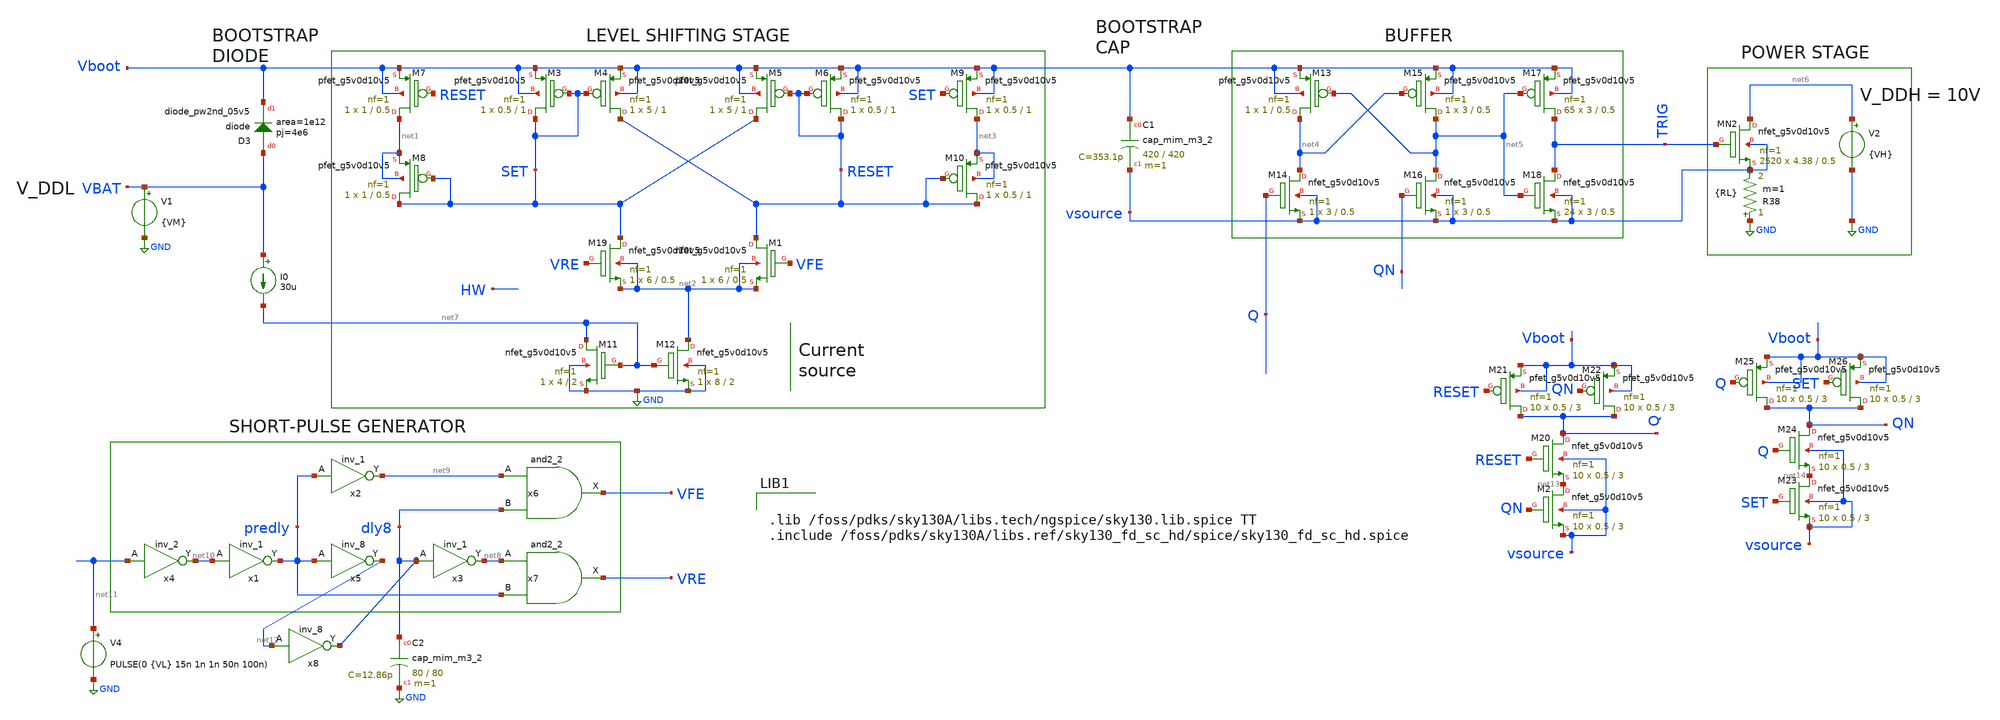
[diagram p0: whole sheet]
** sch_path: LS_boot_20230921/sch/LS_boot_latest_jm.sch
**.subckt LS_boot_latest_jm
XM7 net1 RESET Vboot Vboot sky130_fd_pr__pfet_g5v0d10v5 L=0.5 W=1 nf=1 ad='int((nf+1)/2) * W/nf * 0.29'
+ as='int((nf+2)/2) * W/nf * 0.29' pd='2*int((nf+1)/2) * (W/nf + 0.29)' ps='2*int((nf+2)/2) * (W/nf + 0.29)'
+ nrd='0.29 / W' nrs='0.29 / W' sa=0 sb=0 sd=0 mult=1 m=1
XM8 SET SET net1 net1 sky130_fd_pr__pfet_g5v0d10v5 L=0.5 W=1 nf=1 ad='int((nf+1)/2) * W/nf * 0.29' as='int((nf+2)/2) * W/nf * 0.29'
+ pd='2*int((nf+1)/2) * (W/nf + 0.29)' ps='2*int((nf+2)/2) * (W/nf + 0.29)' nrd='0.29 / W' nrs='0.29 / W'
+ sa=0 sb=0 sd=0 mult=1 m=1
XM4 RESET SET Vboot Vboot sky130_fd_pr__pfet_g5v0d10v5 L=1 W=5 nf=1 ad='int((nf+1)/2) * W/nf * 0.29'
+ as='int((nf+2)/2) * W/nf * 0.29' pd='2*int((nf+1)/2) * (W/nf + 0.29)' ps='2*int((nf+2)/2) * (W/nf + 0.29)'
+ nrd='0.29 / W' nrs='0.29 / W' sa=0 sb=0 sd=0 mult=1 m=1
XM3 SET SET Vboot Vboot sky130_fd_pr__pfet_g5v0d10v5 L=1 W=0.5 nf=1 ad='int((nf+1)/2) * W/nf * 0.29'
+ as='int((nf+2)/2) * W/nf * 0.29' pd='2*int((nf+1)/2) * (W/nf + 0.29)' ps='2*int((nf+2)/2) * (W/nf + 0.29)'
+ nrd='0.29 / W' nrs='0.29 / W' sa=0 sb=0 sd=0 mult=1 m=1
XM9 net3 SET Vboot Vboot sky130_fd_pr__pfet_g5v0d10v5 L=1 W=0.5 nf=1 ad='int((nf+1)/2) * W/nf * 0.29'
+ as='int((nf+2)/2) * W/nf * 0.29' pd='2*int((nf+1)/2) * (W/nf + 0.29)' ps='2*int((nf+2)/2) * (W/nf + 0.29)'
+ nrd='0.29 / W' nrs='0.29 / W' sa=0 sb=0 sd=0 mult=1 m=1
XM10 RESET RESET net3 net3 sky130_fd_pr__pfet_g5v0d10v5 L=1 W=0.5 nf=1 ad='int((nf+1)/2) * W/nf * 0.29'
+ as='int((nf+2)/2) * W/nf * 0.29' pd='2*int((nf+1)/2) * (W/nf + 0.29)' ps='2*int((nf+2)/2) * (W/nf + 0.29)'
+ nrd='0.29 / W' nrs='0.29 / W' sa=0 sb=0 sd=0 mult=1 m=1
XM5 SET RESET Vboot Vboot sky130_fd_pr__pfet_g5v0d10v5 L=1 W=5 nf=1 ad='int((nf+1)/2) * W/nf * 0.29'
+ as='int((nf+2)/2) * W/nf * 0.29' pd='2*int((nf+1)/2) * (W/nf + 0.29)' ps='2*int((nf+2)/2) * (W/nf + 0.29)'
+ nrd='0.29 / W' nrs='0.29 / W' sa=0 sb=0 sd=0 mult=1 m=1
XM6 RESET RESET Vboot Vboot sky130_fd_pr__pfet_g5v0d10v5 L=1 W=0.5 nf=1 ad='int((nf+1)/2) * W/nf * 0.29'
+ as='int((nf+2)/2) * W/nf * 0.29' pd='2*int((nf+1)/2) * (W/nf + 0.29)' ps='2*int((nf+2)/2) * (W/nf + 0.29)'
+ nrd='0.29 / W' nrs='0.29 / W' sa=0 sb=0 sd=0 mult=1 m=1
XD3 VBAT Vboot sky130_fd_pr__diode_pw2nd_05v5 area=1e12 pj=4e6
I0 VBAT net7 30u
x1 net10 VGND VNB VPB VPWR predly sky130_fd_sc_hd__inv_1
x2 predly VGND VNB VPB VPWR net9 sky130_fd_sc_hd__inv_1
x3 dly8 VGND VNB VPB VPWR net8 sky130_fd_sc_hd__inv_1
x4 net11 VGND VNB VPB VPWR net10 sky130_fd_sc_hd__inv_2
x5 predly VGND VNB VPB VPWR net12 sky130_fd_sc_hd__inv_8
x6 net9 dly8 VGND VNB VPB VPWR VFE sky130_fd_sc_hd__and2_2
x7 net8 predly VGND VNB VPB VPWR VRE sky130_fd_sc_hd__and2_2
XC1 Vboot vsource sky130_fd_pr__cap_mim_m3_2 W=420 L=420 MF=1 m=1
XM15 net5 net4 Vboot Vboot sky130_fd_pr__pfet_g5v0d10v5 L=0.5 W=3 nf=1 ad='int((nf+1)/2) * W/nf * 0.29'
+ as='int((nf+2)/2) * W/nf * 0.29' pd='2*int((nf+1)/2) * (W/nf + 0.29)' ps='2*int((nf+2)/2) * (W/nf + 0.29)'
+ nrd='0.29 / W' nrs='0.29 / W' sa=0 sb=0 sd=0 mult=1 m=1
XM13 net4 net5 Vboot Vboot sky130_fd_pr__pfet_g5v0d10v5 L=0.5 W=1 nf=1 ad='int((nf+1)/2) * W/nf * 0.29'
+ as='int((nf+2)/2) * W/nf * 0.29' pd='2*int((nf+1)/2) * (W/nf + 0.29)' ps='2*int((nf+2)/2) * (W/nf + 0.29)'
+ nrd='0.29 / W' nrs='0.29 / W' sa=0 sb=0 sd=0 mult=1 m=1
XM17 TRIG net5 Vboot Vboot sky130_fd_pr__pfet_g5v0d10v5 L=0.5 W=3 nf=1 ad='int((nf+1)/2) * W/nf * 0.29'
+ as='int((nf+2)/2) * W/nf * 0.29' pd='2*int((nf+1)/2) * (W/nf + 0.29)' ps='2*int((nf+2)/2) * (W/nf + 0.29)'
+ nrd='0.29 / W' nrs='0.29 / W' sa=0 sb=0 sd=0 mult=65 m=65
V4 net11 GND PULSE(0 {VL} 15n 1n 1n 50n 100n)
V1 VBAT GND {VM}
XMN2 net6 TRIG vsource vsource sky130_fd_pr__nfet_g5v0d10v5 L=0.5 W=4.38 nf=1 ad='int((nf+1)/2) * W/nf * 0.29'
+ as='int((nf+2)/2) * W/nf * 0.29' pd='2*int((nf+1)/2) * (W/nf + 0.29)' ps='2*int((nf+2)/2) * (W/nf + 0.29)'
+ nrd='0.29 / W' nrs='0.29 / W' sa=0 sb=0 sd=0 mult=2520 m=2520
V2 net6 GND {VH}
R38 GND vsource {RL} m=1
XM11 net7 net7 GND GND sky130_fd_pr__nfet_g5v0d10v5 L=2 W=4 nf=1 ad='int((nf+1)/2) * W/nf * 0.29' as='int((nf+2)/2) * W/nf * 0.29'
+ pd='2*int((nf+1)/2) * (W/nf + 0.29)' ps='2*int((nf+2)/2) * (W/nf + 0.29)' nrd='0.29 / W' nrs='0.29 / W'
+ sa=0 sb=0 sd=0 mult=1 m=1
XM12 net2 net7 GND GND sky130_fd_pr__nfet_g5v0d10v5 L=2 W=8 nf=1 ad='int((nf+1)/2) * W/nf * 0.29' as='int((nf+2)/2) * W/nf * 0.29'
+ pd='2*int((nf+1)/2) * (W/nf + 0.29)' ps='2*int((nf+2)/2) * (W/nf + 0.29)' nrd='0.29 / W' nrs='0.29 / W'
+ sa=0 sb=0 sd=0 mult=1 m=1
XM14 net4 Q vsource vsource sky130_fd_pr__nfet_g5v0d10v5 L=0.5 W=3 nf=1 ad='int((nf+1)/2) * W/nf * 0.29'
+ as='int((nf+2)/2) * W/nf * 0.29' pd='2*int((nf+1)/2) * (W/nf + 0.29)' ps='2*int((nf+2)/2) * (W/nf + 0.29)'
+ nrd='0.29 / W' nrs='0.29 / W' sa=0 sb=0 sd=0 mult=1 m=1
XM16 net5 QN vsource vsource sky130_fd_pr__nfet_g5v0d10v5 L=0.5 W=3 nf=1 ad='int((nf+1)/2) * W/nf * 0.29'
+ as='int((nf+2)/2) * W/nf * 0.29' pd='2*int((nf+1)/2) * (W/nf + 0.29)' ps='2*int((nf+2)/2) * (W/nf + 0.29)'
+ nrd='0.29 / W' nrs='0.29 / W' sa=0 sb=0 sd=0 mult=1 m=1
XM18 TRIG net5 vsource vsource sky130_fd_pr__nfet_g5v0d10v5 L=0.5 W=3 nf=1 ad='int((nf+1)/2) * W/nf * 0.29'
+ as='int((nf+2)/2) * W/nf * 0.29' pd='2*int((nf+1)/2) * (W/nf + 0.29)' ps='2*int((nf+2)/2) * (W/nf + 0.29)'
+ nrd='0.29 / W' nrs='0.29 / W' sa=0 sb=0 sd=0 mult=24 m=24
XM19 SET VRE net2 net2 sky130_fd_pr__nfet_g5v0d10v5 L=0.5 W=6 nf=1 ad='int((nf+1)/2) * W/nf * 0.29' as='int((nf+2)/2) * W/nf * 0.29'
+ pd='2*int((nf+1)/2) * (W/nf + 0.29)' ps='2*int((nf+2)/2) * (W/nf + 0.29)' nrd='0.29 / W' nrs='0.29 / W'
+ sa=0 sb=0 sd=0 mult=1 m=1
XM1 RESET VFE net2 net2 sky130_fd_pr__nfet_g5v0d10v5 L=0.5 W=6 nf=1 ad='int((nf+1)/2) * W/nf * 0.29'
+ as='int((nf+2)/2) * W/nf * 0.29' pd='2*int((nf+1)/2) * (W/nf + 0.29)' ps='2*int((nf+2)/2) * (W/nf + 0.29)'
+ nrd='0.29 / W' nrs='0.29 / W' sa=0 sb=0 sd=0 mult=1 m=1
XM2 net13 QN vsource vsource sky130_fd_pr__nfet_g5v0d10v5 L=3 W=0.5 nf=1 ad='int((nf+1)/2) * W/nf * 0.29'
+ as='int((nf+2)/2) * W/nf * 0.29' pd='2*int((nf+1)/2) * (W/nf + 0.29)' ps='2*int((nf+2)/2) * (W/nf + 0.29)'
+ nrd='0.29 / W' nrs='0.29 / W' sa=0 sb=0 sd=0 mult=10 m=10
XM20 Q RESET net13 vsource sky130_fd_pr__nfet_g5v0d10v5 L=3 W=0.5 nf=1 ad='int((nf+1)/2) * W/nf * 0.29'
+ as='int((nf+2)/2) * W/nf * 0.29' pd='2*int((nf+1)/2) * (W/nf + 0.29)' ps='2*int((nf+2)/2) * (W/nf + 0.29)'
+ nrd='0.29 / W' nrs='0.29 / W' sa=0 sb=0 sd=0 mult=10 m=10
XM21 Q RESET Vboot Vboot sky130_fd_pr__pfet_g5v0d10v5 L=3 W=0.5 nf=1 ad='int((nf+1)/2) * W/nf * 0.29'
+ as='int((nf+2)/2) * W/nf * 0.29' pd='2*int((nf+1)/2) * (W/nf + 0.29)' ps='2*int((nf+2)/2) * (W/nf + 0.29)'
+ nrd='0.29 / W' nrs='0.29 / W' sa=0 sb=0 sd=0 mult=10 m=10
XM22 Q QN Vboot Vboot sky130_fd_pr__pfet_g5v0d10v5 L=3 W=0.5 nf=1 ad='int((nf+1)/2) * W/nf * 0.29' as='int((nf+2)/2) * W/nf * 0.29'
+ pd='2*int((nf+1)/2) * (W/nf + 0.29)' ps='2*int((nf+2)/2) * (W/nf + 0.29)' nrd='0.29 / W' nrs='0.29 / W'
+ sa=0 sb=0 sd=0 mult=10 m=10
XM23 net14 SET vsource vsource sky130_fd_pr__nfet_g5v0d10v5 L=3 W=0.5 nf=1 ad='int((nf+1)/2) * W/nf * 0.29'
+ as='int((nf+2)/2) * W/nf * 0.29' pd='2*int((nf+1)/2) * (W/nf + 0.29)' ps='2*int((nf+2)/2) * (W/nf + 0.29)'
+ nrd='0.29 / W' nrs='0.29 / W' sa=0 sb=0 sd=0 mult=10 m=10
XM24 QN Q net14 vsource sky130_fd_pr__nfet_g5v0d10v5 L=3 W=0.5 nf=1 ad='int((nf+1)/2) * W/nf * 0.29'
+ as='int((nf+2)/2) * W/nf * 0.29' pd='2*int((nf+1)/2) * (W/nf + 0.29)' ps='2*int((nf+2)/2) * (W/nf + 0.29)'
+ nrd='0.29 / W' nrs='0.29 / W' sa=0 sb=0 sd=0 mult=10 m=10
XM25 QN Q Vboot Vboot sky130_fd_pr__pfet_g5v0d10v5 L=3 W=0.5 nf=1 ad='int((nf+1)/2) * W/nf * 0.29' as='int((nf+2)/2) * W/nf * 0.29'
+ pd='2*int((nf+1)/2) * (W/nf + 0.29)' ps='2*int((nf+2)/2) * (W/nf + 0.29)' nrd='0.29 / W' nrs='0.29 / W'
+ sa=0 sb=0 sd=0 mult=10 m=10
XM26 QN SET Vboot Vboot sky130_fd_pr__pfet_g5v0d10v5 L=3 W=0.5 nf=1 ad='int((nf+1)/2) * W/nf * 0.29'
+ as='int((nf+2)/2) * W/nf * 0.29' pd='2*int((nf+1)/2) * (W/nf + 0.29)' ps='2*int((nf+2)/2) * (W/nf + 0.29)'
+ nrd='0.29 / W' nrs='0.29 / W' sa=0 sb=0 sd=0 mult=10 m=10
XC2 dly8 GND sky130_fd_pr__cap_mim_m3_2 W=80 L=80 MF=1 m=1
x8 net12 VGND VNB VPB VPWR dly8 sky130_fd_sc_hd__inv_8
**** begin user architecture code


.lib /foss/pdks/sky130A/libs.tech/ngspice/sky130.lib.spice TT
.include /foss/pdks/sky130A/libs.ref/sky130_fd_sc_hd/spice/sky130_fd_sc_hd.spice




VGND VGND GND 0
VNB VNB GND 0
VPB VPB GND 1.8
VPWR VPWR GND 1.8
.param VH = 10
.param VM = 5
.param VL = 1.8
.param RL = 50
.option scale=1e-6
*.option temp=70
*.probe vd(MP2:G:S)

.param mc_mm_switch=0

.options savecurrents
.control
save all
tran 100n 5u
write /foss/designs/Open3LFCC_V2/LS_boot_20230921/sch/LS_BOOT.raw

plot v(trig) - v(vsource)
.endc


**** end user architecture code
**.ends
.GLOBAL GND
.end
